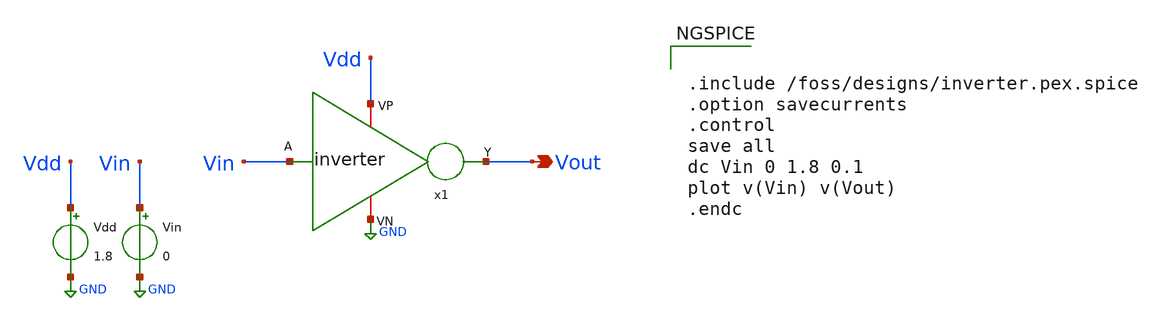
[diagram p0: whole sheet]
** sch_path: Familiarization_of_Opensource_Design_Flow/inverter_dc_tb.sch
**.subckt inverter_dc_tb Vout
*.opin Vout
x1 Vdd Vin Vout GND inverter
Vdd Vdd GND 1.8
Vin Vin GND 0
**** begin user architecture code

** opencircuitdesign pdks install
.lib $::SKYWATER_MODELS/sky130.lib.spice tt



.include /foss/designs/inverter.pex.spice
.option savecurrents
.control
save all
dc Vin 0 1.8 0.1
plot v(Vin) v(Vout)
.endc


**** end user architecture code
**.ends
.GLOBAL GND
.end
